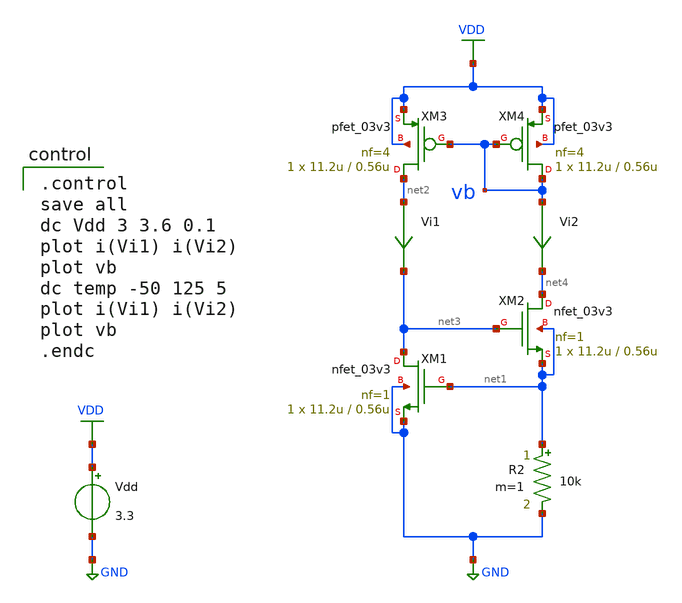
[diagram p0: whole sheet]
** sch_path: current-source/cs-vth-ref.sch
**.subckt cs-vth-ref
Vdd VDD GND 3.3
XM1 net3 net1 GND GND nfet_03v3 L=0.56u W=11.2u nf=1 ad='int((nf+1)/2) * W/nf * 0.18u' as='int((nf+2)/2) * W/nf * 0.18u'
+ pd='2*int((nf+1)/2) * (W/nf + 0.18u)' ps='2*int((nf+2)/2) * (W/nf + 0.18u)' nrd='0.18u / W' nrs='0.18u / W'
+ sa=0 sb=0 sd=0 m=1
XM2 net4 net3 net1 net1 nfet_03v3 L=0.56u W=11.2u nf=1 ad='int((nf+1)/2) * W/nf * 0.18u' as='int((nf+2)/2) * W/nf * 0.18u'
+ pd='2*int((nf+1)/2) * (W/nf + 0.18u)' ps='2*int((nf+2)/2) * (W/nf + 0.18u)' nrd='0.18u / W' nrs='0.18u / W'
+ sa=0 sb=0 sd=0 m=1
Vi1 net2 net3 0
.save i(vi1)
Vi2 vb net4 0
.save i(vi2)
R2 net1 GND 10k m=1
XM3 net2 vb VDD VDD pfet_03v3 L=0.56u W=11.2u nf=4 ad='int((nf+1)/2) * W/nf * 0.18u' as='int((nf+2)/2) * W/nf * 0.18u'
+ pd='2*int((nf+1)/2) * (W/nf + 0.18u)' ps='2*int((nf+2)/2) * (W/nf + 0.18u)' nrd='0.18u / W' nrs='0.18u / W'
+ sa=0 sb=0 sd=0 m=1
XM4 vb vb VDD VDD pfet_03v3 L=0.56u W=11.2u nf=4 ad='int((nf+1)/2) * W/nf * 0.18u' as='int((nf+2)/2) * W/nf * 0.18u'
+ pd='2*int((nf+1)/2) * (W/nf + 0.18u)' ps='2*int((nf+2)/2) * (W/nf + 0.18u)' nrd='0.18u / W' nrs='0.18u / W'
+ sa=0 sb=0 sd=0 m=1
**** begin user architecture code

.include $::180MCU_MODELS/design.ngspice
.lib $::180MCU_MODELS/sm141064.ngspice typical
.lib $::180MCU_MODELS/sm141064.ngspice res_typical
.lib $::180MCU_MODELS/sm141064.ngspice moscap_typical
.lib $::180MCU_MODELS/sm141064.ngspice bjt_typical
* .lib $::180MCU_MODELS/sm141064.ngspice res_statistical


.control
save all
dc Vdd 3 3.6 0.1
plot i(Vi1) i(Vi2)
plot vb
dc temp -50 125 5
plot i(Vi1) i(Vi2)
plot vb
.endc

**** end user architecture code
**.ends
.GLOBAL GND
.GLOBAL VDD
.end
